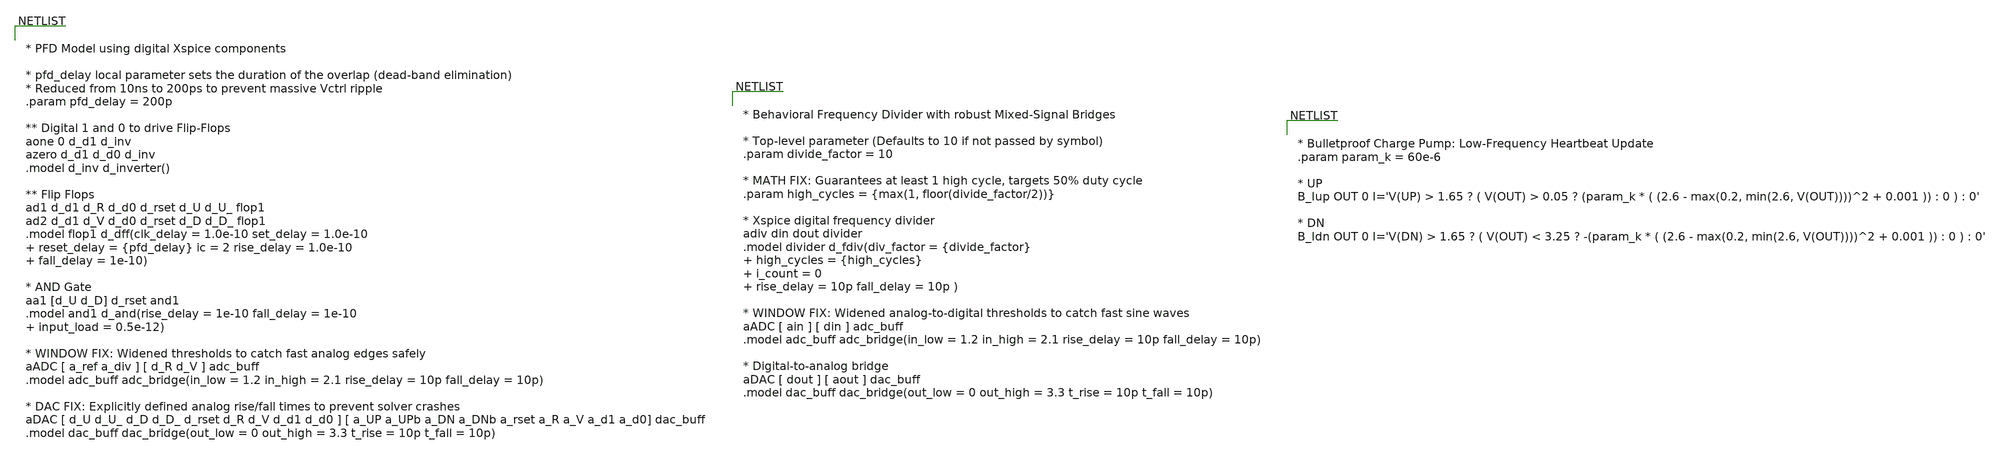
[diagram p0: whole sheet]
** sch_path: designs/untitled.sch
**.subckt untitled
**** begin user architecture code


* PFD Model using digital Xspice components

* pfd_delay local parameter sets the duration of the overlap (dead-band elimination)
* Reduced from 10ns to 200ps to prevent massive Vctrl ripple
.param pfd_delay = 200p

** Digital 1 and 0 to drive Flip-Flops
aone 0 d_d1 d_inv
azero d_d1 d_d0 d_inv
.model d_inv d_inverter()

** Flip Flops
ad1 d_d1 d_R d_d0 d_rset d_U d_U_ flop1
ad2 d_d1 d_V d_d0 d_rset d_D d_D_ flop1
.model flop1 d_dff(clk_delay = 1.0e-10 set_delay = 1.0e-10  reset_delay = {pfd_delay} ic = 2 rise_delay
+ = 1.0e-10  fall_delay = 1e-10)

* AND Gate
aa1 [d_U d_D] d_rset and1
.model and1 d_and(rise_delay = 1e-10 fall_delay = 1e-10   input_load = 0.5e-12)

* WINDOW FIX: Widened thresholds to catch fast analog edges safely
aADC [ a_ref a_div ] [ d_R d_V ] adc_buff
.model adc_buff adc_bridge(in_low = 1.2 in_high = 2.1 rise_delay = 10p fall_delay = 10p)

* DAC FIX: Explicitly defined analog rise/fall times to prevent solver crashes
aDAC [ d_U d_U_ d_D d_D_ d_rset d_R d_V d_d1 d_d0 ] [ a_UP a_UPb a_DN a_DNb a_rset a_R a_V a_d1
+ a_d0] dac_buff
.model dac_buff dac_bridge(out_low = 0 out_high = 3.3 t_rise = 10p t_fall = 10p)




* Behavioral Frequency Divider with robust Mixed-Signal Bridges

* Top-level parameter (Defaults to 10 if not passed by symbol)
.param divide_factor = 10

* MATH FIX: Guarantees at least 1 high cycle, targets 50% duty cycle
.param high_cycles = {max(1, floor(divide_factor/2))}

* Xspice digital frequency divider
adiv din dout divider
.model divider d_fdiv(div_factor = {divide_factor}  high_cycles = {high_cycles}  i_count = 0  rise_delay
+ = 10p fall_delay = 10p )

* WINDOW FIX: Widened analog-to-digital thresholds to catch fast sine waves
aADC [ ain ] [ din ] adc_buff
.model adc_buff adc_bridge(in_low = 1.2 in_high = 2.1 rise_delay = 10p fall_delay = 10p)

* Digital-to-analog bridge
aDAC [ dout ] [ aout ] dac_buff
.model dac_buff dac_bridge(out_low = 0 out_high = 3.3 t_rise = 10p t_fall = 10p)




* Bulletproof Charge Pump: Low-Frequency Heartbeat Update
.param param_k = 60e-6

* UP
B_Iup OUT 0 I='V(UP) > 1.65 ? ( V(OUT) > 0.05 ? (param_k * ( (2.6 - max(0.2, min(2.6, V(OUT))))^2 + 0.001 )) : 0 ) : 0'

* DN
B_Idn OUT 0 I='V(DN) > 1.65 ? ( V(OUT) < 3.25 ? -(param_k * ( (2.6 - max(0.2, min(2.6, V(OUT))))^2 + 0.001 )) : 0 ) : 0'


**** end user architecture code
**.ends
.end
